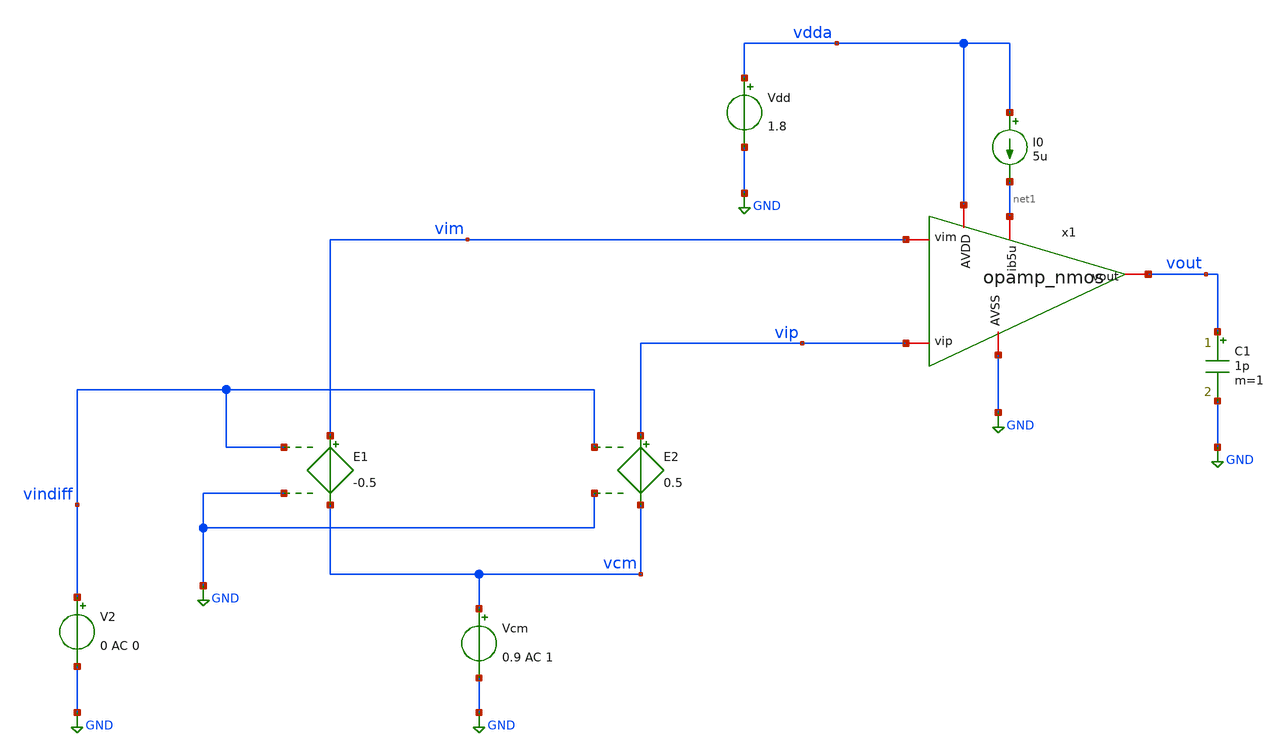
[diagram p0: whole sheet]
** sch_path: xschem/TB_opa_nmos1.sch
**.subckt TB_opa_nmos1
E2 vip vcm vindiff GND 0.5
E1 vim vcm vindiff GND -0.5
Vcm vcm GND 0.9 AC 1
V2 vindiff GND 0 AC 0
x1 vip GND vdda vim net1 vout opamp_nmos
Vdd vdda GND 1.8
I0 vdda net1 5u
C1 vout GND 1p m=1
**** begin user architecture code

** opencircuitdesign pdks install
.lib $::SKYWATER_MODELS/sky130.lib.spice tt




* ngspice commands
.temp 27
.control

 save all

 save @m.x1.xm1.msky130_fd_pr__nfet_01v8[id]
 save @m.x1.xm1.msky130_fd_pr__nfet_01v8[gm]

 save @m.x1.xmim.msky130_fd_pr__nfet_01v8_lvt[id]
 save @m.x1.xmim.msky130_fd_pr__nfet_01v8_lvt[gm]

 save @m.x1.xmip.msky130_fd_pr__nfet_01v8_lvt[id]
 save @m.x1.xmip.msky130_fd_pr__nfet_01v8_lvt[gm]

 save @m.x1.xmpcmm.msky130_fd_pr__pfet_01v8_lvt[id]
 save @m.x1.xmpcmm.msky130_fd_pr__pfet_01v8_lvt[gm]

 save @m.x1.xmpcmp.msky130_fd_pr__pfet_01v8_lvt[id]
 save @m.x1.xmpcmp.msky130_fd_pr__pfet_01v8_lvt[gm]

 save @m.x1.xmtail.msky130_fd_pr__nfet_01v8[id]
 save @m.x1.xmtail.msky130_fd_pr__nfet_01v8[gm]

 OP

 write TB_opa_nmos1.raw

 let im1=@m.x1.xm1.msky130_fd_pr__nfet_01v8[id]
 let iim=@m.x1.xmim.msky130_fd_pr__nfet_01v8_lvt[id]
 let iip=@m.x1.xmip.msky130_fd_pr__nfet_01v8_lvt[id]
 let icmm=@m.x1.xmpcmm.msky130_fd_pr__pfet_01v8_lvt[id]
 let icmp=@m.x1.xmpcmp.msky130_fd_pr__pfet_01v8_lvt[id]
 let imtail=@m.x1.xmtail.msky130_fd_pr__nfet_01v8[id]

 let gm1=@m.x1.xm1.msky130_fd_pr__nfet_01v8[gm]
 let gmim=@m.x1.xmim.msky130_fd_pr__nfet_01v8_lvt[gm]
 let gmip=@m.x1.xmip.msky130_fd_pr__nfet_01v8_lvt[gm]
 let gmcmm=@m.x1.xmpcmm.msky130_fd_pr__pfet_01v8_lvt[gm]
 let gmcmp=@m.x1.xmpcmp.msky130_fd_pr__pfet_01v8_lvt[gm]
 let gmtail=@m.x1.xmtail.msky130_fd_pr__nfet_01v8[gm]

 let gmidm1=gm1/im1
 let gmidim=gmim/iim
 let gmidip=gmip/iip
 let gmidcmm=gmcmm/icmm
 let gmidcmp=gmcmp/icmp
 let gmidtail=gmtail/imtail

 print gmidm1
 print gmidim
 print gmidip
 print gmidcmm
 print gmidcmp
 print gmidtail

 print im1
 print iim
 print iip
 print icmm
 print icmp
 print imtail

 AC DEC 100 1 1e9
 set appendwrite
 write TB_opa_nmos1.raw
 plot vdb(vout)
 plot v(vout)

.endc
.end



**** end user architecture code
**.ends

* expanding   symbol:  opamp_nmos.sym # of pins=6
** sym_path: xschem/opamp_nmos.sym
** sch_path: xschem/opamp_nmos.sch
.subckt opamp_nmos vip AVSS AVDD vim ib5u vout
*.iopin vip
*.iopin vim
*.iopin vout
*.iopin AVDD
*.iopin ib5u
*.iopin AVSS
XMip vom vip net1 net1 sky130_fd_pr__nfet_01v8_lvt L=2 W=5 nf=1 ad='int((1 + 1)/2) * 5 / 1 * 0.29' as='int((1 + 2)/2) * 5 / 1 * 0.29'
+ pd='2*int((1 + 1)/2) * (5 / 1 + 0.29)' ps='2*int((1 + 2)/2) * (5 / 1 + 0.29)' nrd='0.29 / 5 ' nrs='0.29 / 5 '
+ sa=0 sb=0 sd=0 mult=4 m=4
XMim vout vim net1 net1 sky130_fd_pr__nfet_01v8_lvt L=2 W=5 nf=1 ad='int((1 + 1)/2) * 5 / 1 * 0.29' as='int((1 + 2)/2) * 5 / 1 * 0.29'
+ pd='2*int((1 + 1)/2) * (5 / 1 + 0.29)' ps='2*int((1 + 2)/2) * (5 / 1 + 0.29)' nrd='0.29 / 5 ' nrs='0.29 / 5 '
+ sa=0 sb=0 sd=0 mult=4 m=4
XM1 ib5u ib5u AVSS AVSS sky130_fd_pr__nfet_01v8 L=1 W=5 nf=1 ad='int((1 + 1)/2) * 5 / 1 * 0.29' as='int((1 + 2)/2) * 5 / 1 * 0.29'
+ pd='2*int((1 + 1)/2) * (5 / 1 + 0.29)' ps='2*int((1 + 2)/2) * (5 / 1 + 0.29)' nrd='0.29 / 5 ' nrs='0.29 / 5 '
+ sa=0 sb=0 sd=0 mult=1 m=1
XMtail net1 ib5u AVSS AVSS sky130_fd_pr__nfet_01v8 L=1 W=5 nf=1 ad='int((1 + 1)/2) * 5 / 1 * 0.29' as='int((1 + 2)/2) * 5 / 1 * 0.29'
+ pd='2*int((1 + 1)/2) * (5 / 1 + 0.29)' ps='2*int((1 + 2)/2) * (5 / 1 + 0.29)' nrd='0.29 / 5 ' nrs='0.29 / 5 '
+ sa=0 sb=0 sd=0 mult=2 m=2
XMpcmp vom vom AVDD AVDD sky130_fd_pr__pfet_01v8_lvt L=2 W=5 nf=1 ad='int((1 + 1)/2) * 5 / 1 * 0.29'
+ as='int((1 + 2)/2) * 5 / 1 * 0.29' pd='2*int((1 + 1)/2) * (5 / 1 + 0.29)' ps='2*int((1 + 2)/2) * (5 / 1 + 0.29)'
+ nrd='0.29 / 5 ' nrs='0.29 / 5 ' sa=0 sb=0 sd=0 mult=2 m=2
XMpcmm vout vom AVDD AVDD sky130_fd_pr__pfet_01v8_lvt L=2 W=5 nf=1 ad='int((1 + 1)/2) * 5 / 1 * 0.29'
+ as='int((1 + 2)/2) * 5 / 1 * 0.29' pd='2*int((1 + 1)/2) * (5 / 1 + 0.29)' ps='2*int((1 + 2)/2) * (5 / 1 + 0.29)'
+ nrd='0.29 / 5 ' nrs='0.29 / 5 ' sa=0 sb=0 sd=0 mult=2 m=2
.ends

.GLOBAL GND
.end
